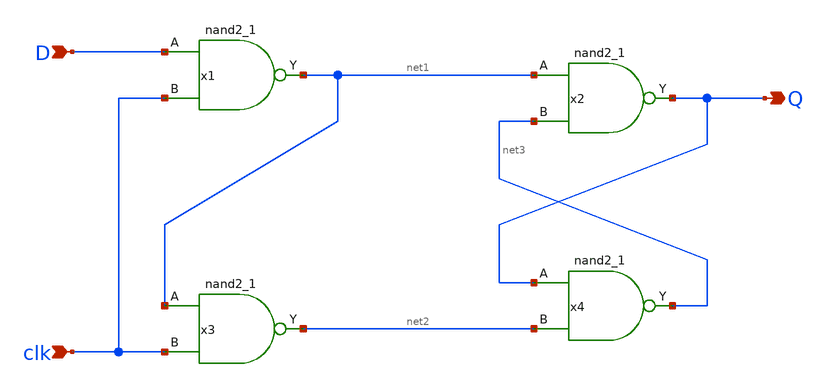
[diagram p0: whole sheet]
** sch_path: xschem/comparator/transparentlatch.sch
**.subckt transparentlatch D clk Q
*.ipin D
*.ipin clk
*.opin Q
x1 D clk GND GND VDD VDD net1 sky130_fd_sc_lp__nand2_1
x2 net1 net3 GND GND VDD VDD Q sky130_fd_sc_lp__nand2_1
x3 net1 clk GND GND VDD VDD net2 sky130_fd_sc_lp__nand2_1
x4 Q net2 GND GND VDD VDD net3 sky130_fd_sc_lp__nand2_1
**.ends
.end
